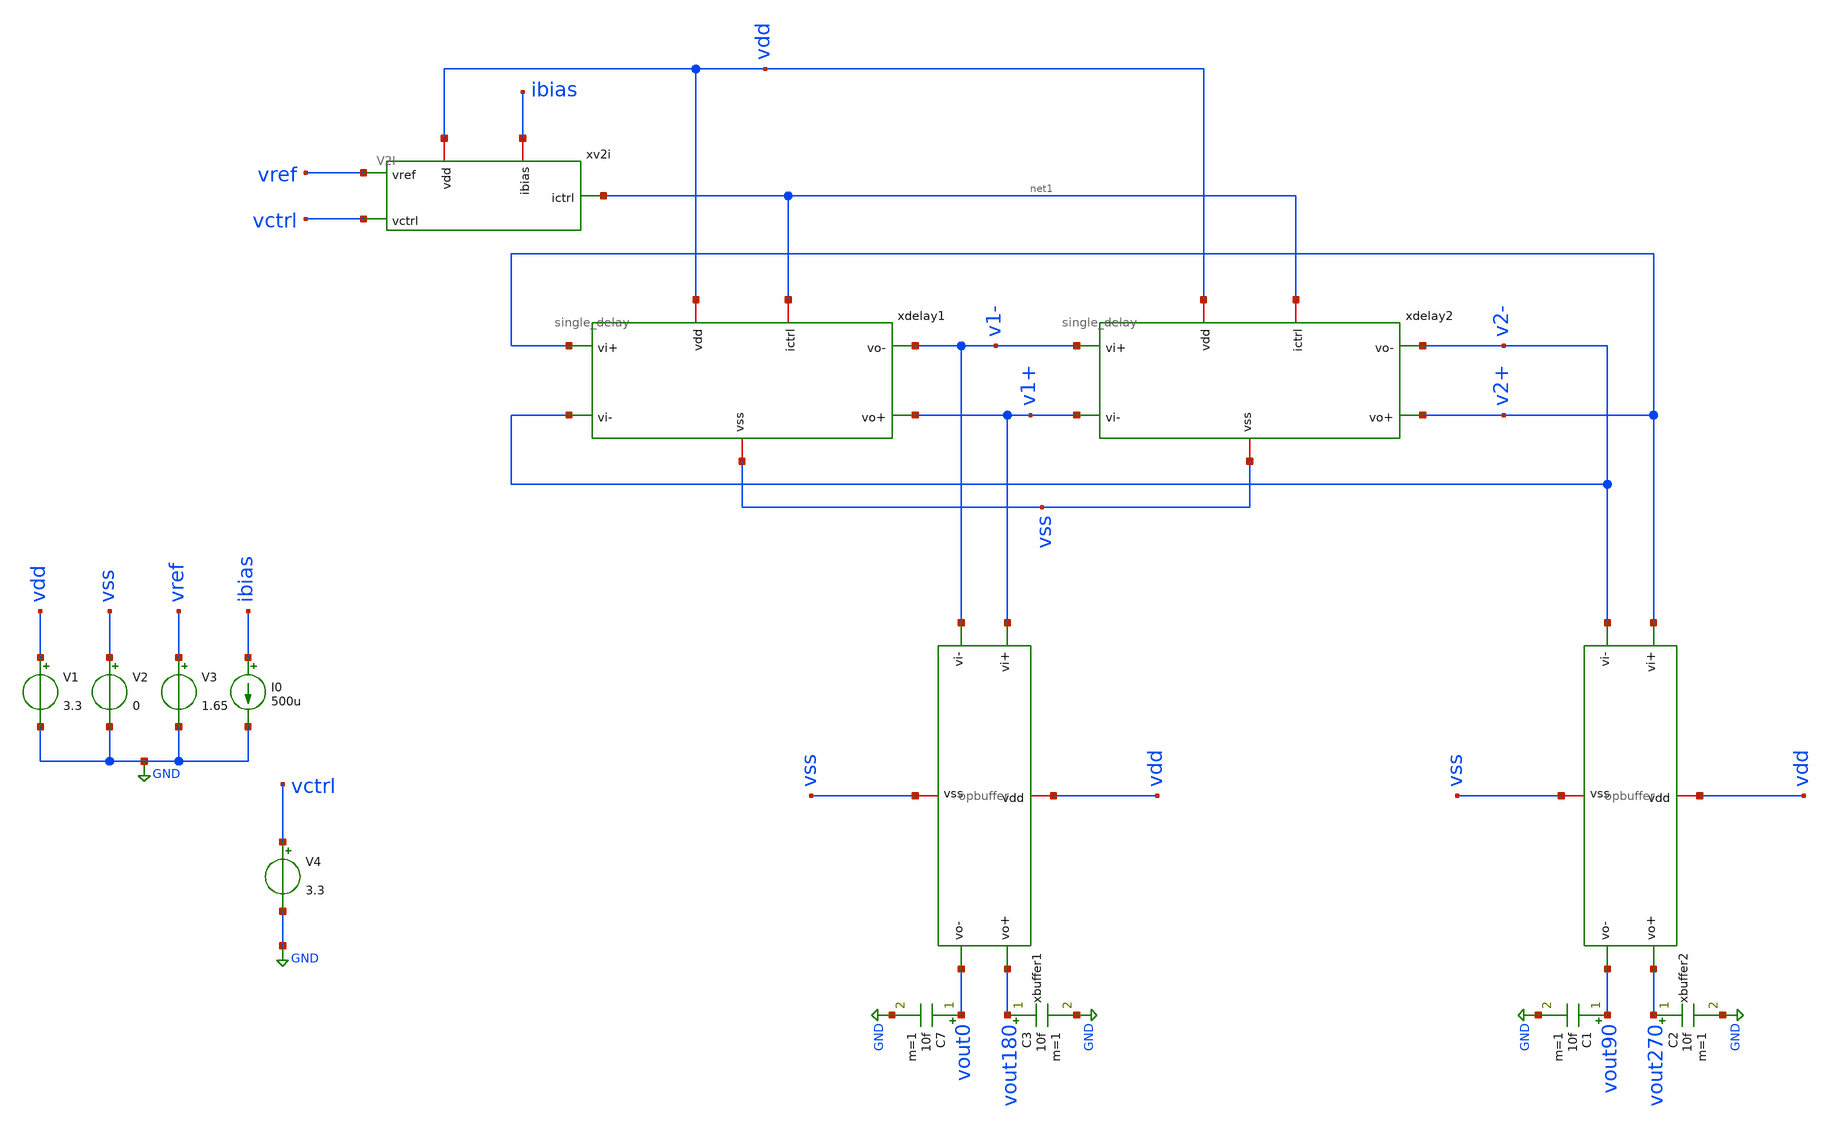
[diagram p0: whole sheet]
** sch_path: xschem/tb.sch
**.subckt tb
xdelay1 net1 vdd v2+ v2- v1- v1+ vss single_delay
xdelay2 net1 vdd v1- v1+ v2- v2+ vss single_delay
xv2i vdd net1 vref vctrl ibias V2I
xbuffer2 vdd vss v2+ vout270 vout90 v2- opbuffer
V1 vdd GND 3.3
V2 vss GND 0
V3 vref GND 1.65
I0 ibias GND 500u
V4 vctrl GND 3.3
xbuffer1 vdd vss v1+ vout180 vout0 v1- opbuffer
C7 vout0 GND 10f m=1
C1 vout90 GND 10f m=1
C2 vout270 GND 10f m=1
C3 vout180 GND 10f m=1
**** begin user architecture code

.include $::180MCU_MODELS/design.ngspice
.lib $::180MCU_MODELS/sm141064.ngspice typical
.lib $::180MCU_MODELS/sm141064.ngspice cap_mim
.lib $::180MCU_MODELS/sm141064.ngspice res_typical
.lib $::180MCU_MODELS/sm141064.ngspice mimcap_typical



.control
let start_v = 0.5
let stop_v  = 3.3
let step_v  = 0.05

let vctrl = start_v

let v_sweep = unitvec(57)
let freq_results = unitvec(57)
let i = 0

dowhile vctrl <= stop_v
	alter @V4[DC] = vctrl
	tran 10p 50n
	meas tran t1 WHEN v(vout0)=1.65 FALL=10
	meas tran t2 WHEN v(vout0)=1.65 FALL=11
	let freq = 1 / (t2 - t1)
	let v_sweep[i] = $&vctrl
	let freq_results[i] = freq
	print freq
	let vctrl = vctrl + step_v
	let i = i + 1
	reset
end
set nolegend
print freq_results
set filetype=ascii
write /foss/designs/vco_des/xschem/freq.txt freq_results
.endc


**** end user architecture code
**.ends
.GLOBAL GND
.end
